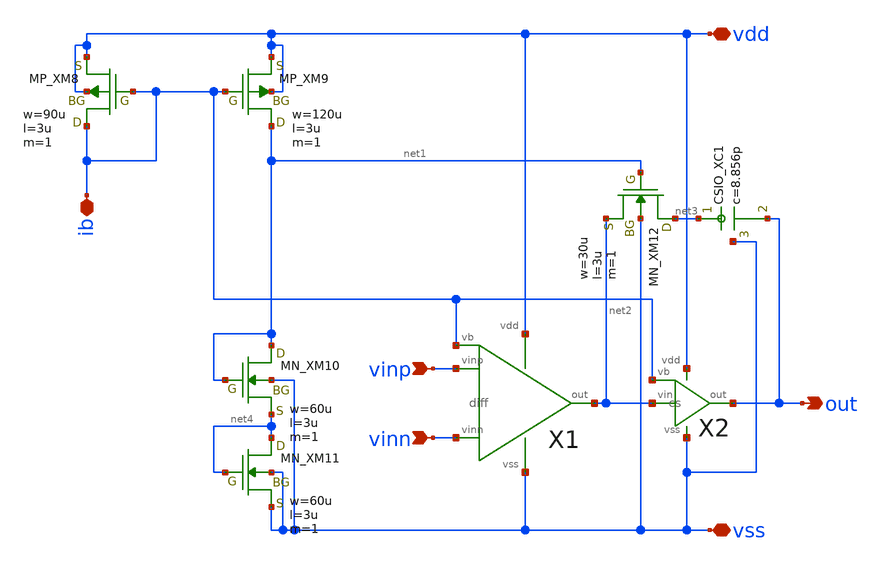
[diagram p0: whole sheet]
** sch_path: member_project/OPAMP/ShuntaroOhno/xschem/opamp.sch
**.subckt opamp vinp vinn out vdd vss ib
*.ipin vinp
*.ipin vinn
*.opin out
*.iopin vdd
*.iopin vss
*.iopin ib
X1 vinp vinn net2 vdd vss ib diff
X2 net2 ib out vdd vss cs
XM9 net1 ib vdd vdd PMOS w=120u l=3u as=0 ad=0 ps=0 pd=0 nrd=0 nrs=0 m=1
XM12 net3 net1 net2 vss NMOS w=30u l=3u as=0 ad=0 ps=0 pd=0 nrd=0 nrs=0 m=1
XM8 ib ib vdd vdd PMOS w=90u l=3u as=0 ad=0 ps=0 pd=0 nrd=0 nrs=0 m=1
XM10 net1 net1 net4 vss NMOS w=60u l=3u as=0 ad=0 ps=0 pd=0 nrd=0 nrs=0 m=1
XM11 net4 net4 vss vss NMOS w=60u l=3u as=0 ad=0 ps=0 pd=0 nrd=0 nrs=0 m=1
XC1 net3 out vss F_CSIO c=8.856p x=120u y=120u m=1
**.ends

* expanding   symbol:  diff.sym # of pins=6
** sym_path: diff.sym
** sch_path: diff.sch
.subckt diff vinp vinn out vdd vss vb
*.ipin vinn
*.ipin vinp
*.ipin vb
*.opin out
*.iopin vdd
*.iopin vss
XM5 net2 vb vdd vdd PMOS w=240u l=3u as=0 ad=0 ps=0 pd=0 nrd=0 nrs=0 m=1
XM1 net1 vinn net2 net2 PMOS w=720u l=3u as=0 ad=0 ps=0 pd=0 nrd=0 nrs=0 m=1
XM2 out vinp net2 net2 PMOS w=720u l=3u as=0 ad=0 ps=0 pd=0 nrd=0 nrs=0 m=1
XM3 net1 net1 vss vss NMOS w=60u l=3u as=0 ad=0 ps=0 pd=0 nrd=0 nrs=0 m=1
XM4 out net1 vss vss NMOS w=60u l=3u as=0 ad=0 ps=0 pd=0 nrd=0 nrs=0 m=1
.ends


* expanding   symbol:  cs.sym # of pins=5
** sym_path: cs.sym
** sch_path: cs.sch
.subckt cs vin vb out vdd vss
*.ipin vb
*.ipin vin
*.opin out
*.iopin vss
*.iopin vdd
XM6 out vb vdd vdd PMOS w=540u l=3u as=0 ad=0 ps=0 pd=0 nrd=0 nrs=0 m=1
XM7 out vin vss vss NMOS w=270u l=3u as=0 ad=0 ps=0 pd=0 nrd=0 nrs=0 m=1
.ends

.end
